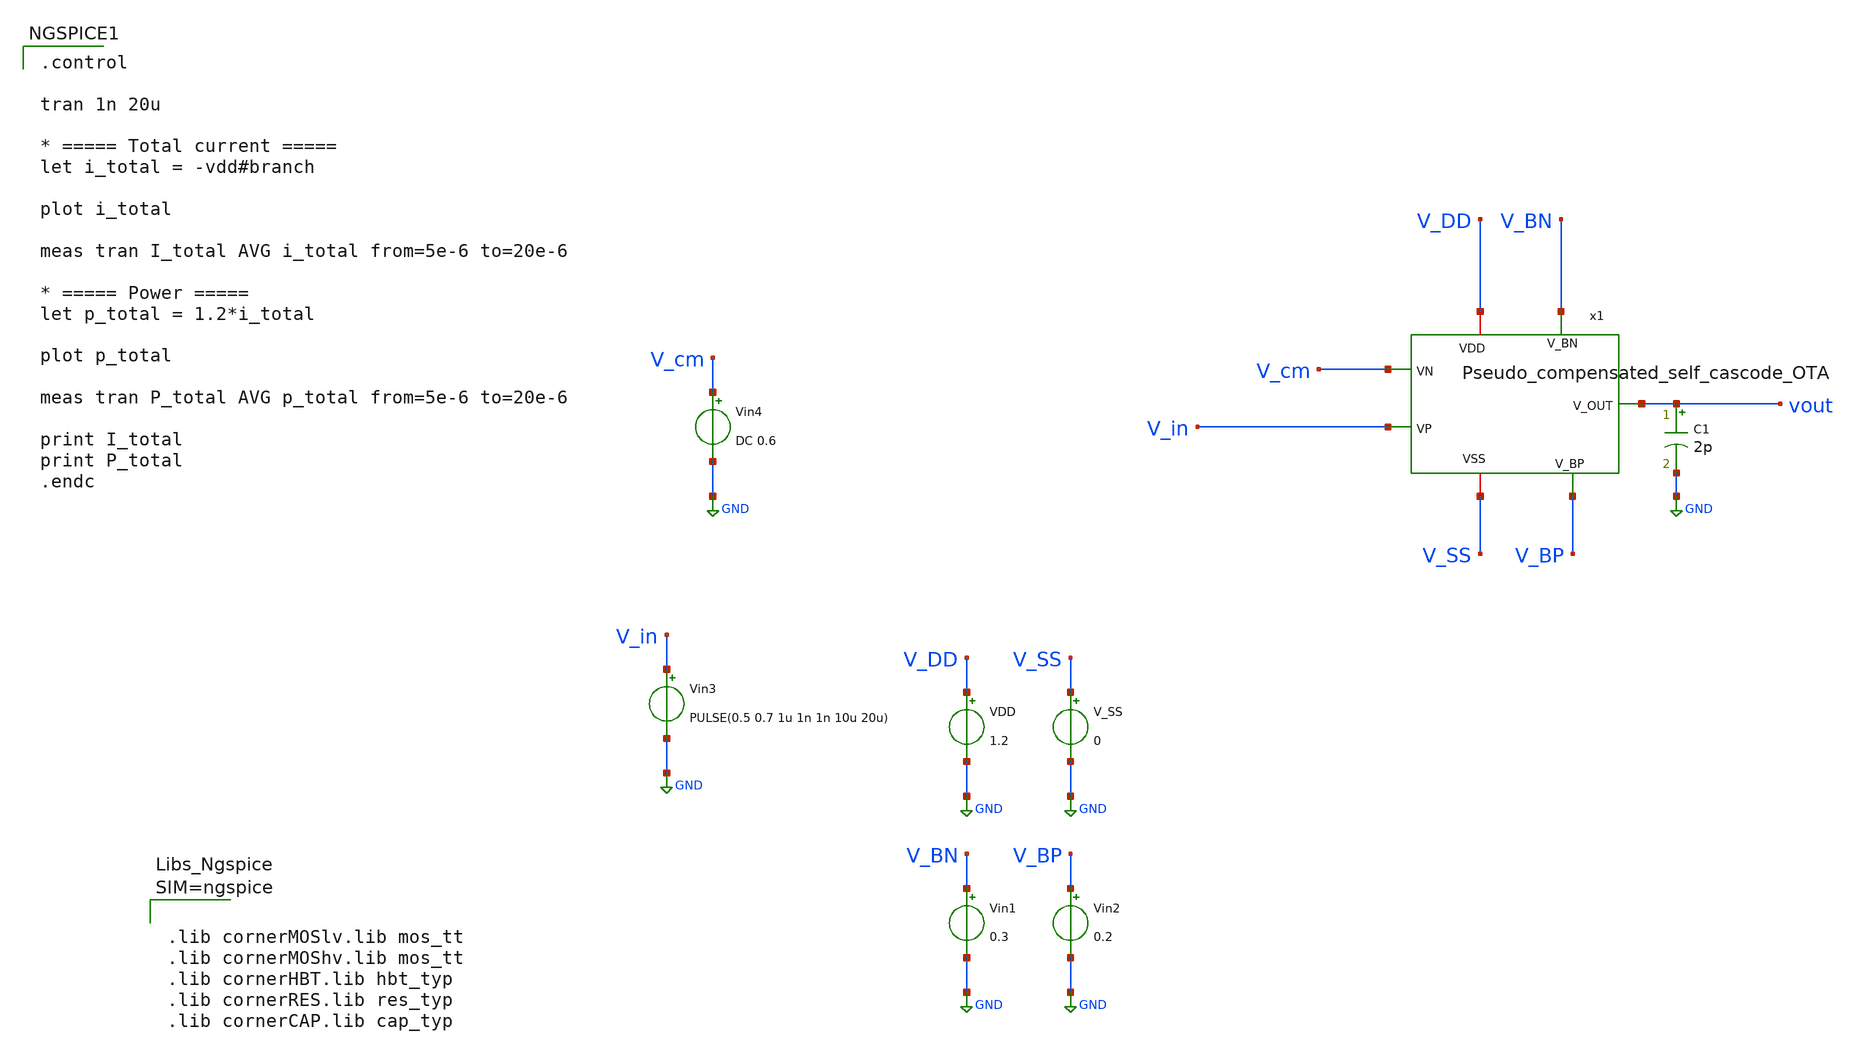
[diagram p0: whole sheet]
** sch_path: xschem/OTA_tb_power_consumption.sch
**.subckt OTA_tb_power_consumption
VDD V_DD GND 1.2
V_SS V_SS GND 0
Vin1 V_BN GND 0.3
Vin2 V_BP GND 0.2
x1 V_cm V_in V_BN V_BP vout V_DD V_SS Pseudo_compensated_self_cascode_OTA
C1 vout GND 2p m=1
Vin3 V_in GND PULSE(0.5 0.7 1u 1n 1n 10u 20u)
Vin4 V_cm GND DC 0.6
**** begin user architecture code

.control

tran 1n 20u

* ===== Total current =====
let i_total = -vdd#branch

plot i_total

meas tran I_total AVG i_total from=5e-6 to=20e-6

* ===== Power =====
let p_total = 1.2*i_total

plot p_total

meas tran P_total AVG p_total from=5e-6 to=20e-6

print I_total
print P_total
.endc





.lib cornerMOSlv.lib mos_tt
.lib cornerMOShv.lib mos_tt
.lib cornerHBT.lib hbt_typ
.lib cornerRES.lib res_typ
.lib cornerCAP.lib cap_typ



**** end user architecture code
**.ends

* expanding   symbol:  Pseudo_compensated_self_cascode_OTA.sym # of pins=7
** sym_path: xschem/Pseudo_compensated_self_cascode_OTA.sym
** sch_path: xschem/Pseudo_compensated_self_cascode_OTA.sch
.subckt Pseudo_compensated_self_cascode_OTA VN VP V_BN V_BP V_OUT VDD VSS
*.ipin VN
*.ipin VP
*.ipin V_BN
*.ipin V_BP
*.opin V_OUT
*.iopin VDD
*.iopin VSS
XM11 net1 VN net2 VSS sg13_lv_nmos w=70u l=0.8u ng=7 m=1 mm_ok=1
XM12 V_GS VN net1 V_BP sg13_lv_nmos w=38.5u l=0.3u ng=4 m=1 mm_ok=1
XM21 net4 VP net2 VSS sg13_lv_nmos w=70u l=0.8u ng=7 m=1 mm_ok=1
XM22 VB32 VP net4 V_BP sg13_lv_nmos w=38.5u l=0.3u ng=4 m=1 mm_ok=1
XM52 net2 V_BN net3 V_BN sg13_lv_nmos w=40u l=0.5u ng=4 m=1 mm_ok=1
XM51 net3 V_BN VSS VSS sg13_lv_nmos w=40u l=2.5u ng=4 m=1 mm_ok=1
XM32 V_GS V_GS VS32 VB32 sg13_lv_pmos w=48.5u l=1.24u ng=5 m=1 mm_ok=1
XM31 VS32 V_GS VDD VDD sg13_lv_pmos w=48.5u l=0.87u ng=5 m=1 mm_ok=1
XM42 VB32 V_GS VS42 V_GS sg13_lv_pmos w=48.5u l=1.24u ng=5 m=1 mm_ok=1
XM41 VS42 V_GS VDD VDD sg13_lv_pmos w=48.5u l=0.87u ng=5 m=1 mm_ok=1
XM61 net5 VB32 VDD VDD sg13_lv_pmos w=60u l=0.13u ng=6 m=1 mm_ok=1
XM62 V_OUT VB32 net5 V_BP sg13_lv_pmos w=60u l=0.13u ng=6 m=1 mm_ok=1
XM72 V_OUT V_BN net6 V_BN sg13_lv_nmos w=40u l=0.5u ng=10 m=1 mm_ok=1
XM71 net6 V_BN VSS VSS sg13_lv_nmos w=40u l=2.5u ng=4 m=1 mm_ok=1
XC3 VS42 V_OUT cap_cmim w=5.0e-6 l=5.0e-6 m=38 mm_ok=1
XC1 net4 V_OUT cap_cmim w=5.0e-6 l=5.0e-6 m=38 mm_ok=1
.ends

.GLOBAL GND
.end
